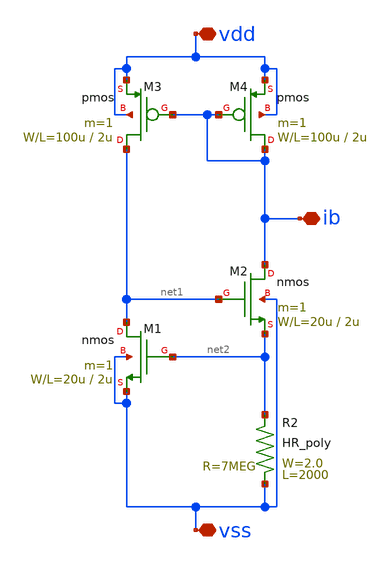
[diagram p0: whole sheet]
** sch_path: OR1/PTC06/opamp/cs-vth-ref_sym.sch
**.subckt cs-vth-ref_sym vdd vss ib
*.iopin vdd
*.iopin vss
*.iopin ib
R2 vss net2 HR_poly W=2.0 L=2000
M4 ib ib vdd vdd pmos L=2u W=100u m=1
M3 net1 ib vdd vdd pmos L=2u W=100u m=1
M2 ib net1 net2 vss nmos L=2u W=20u m=1
M1 net1 net2 vss vss nmos L=2u W=20u m=1
**.ends
.end
